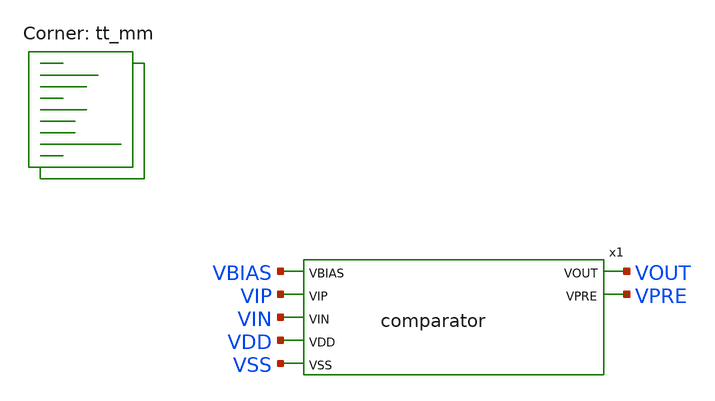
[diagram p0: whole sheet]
** sch_path: xsch/tb_comparator.sch
**.subckt tb_comparator
x1 VBIAS VOUT VIP VPRE VIN VDD VSS comparator
**** begin user architecture code
.lib $::SKYWATER_MODELS/sky130.lib.spice tt_mm

.option method=gear
.option wnflag=1
.option savecurrents

.param VDDGAUSS = agauss(1.8, 0.05, 1)
.param VDD = 'VDDGAUSS'

*.param VBIASGAUSS = agauss(0.7, 0.05, 1)
*.param VBIAS = 'VBIASGAUSS'

.param TEMPGAUSS = agauss(40, 30, 1)
.option temp = 'TEMPGAUSS'

.include stimuli_comparator.cir

Vvdd VDD VSS DC 'VDDGAUSS'

.control
  option seed=9
  let run = 0

  dowhile run < 50
    save all
    save @m5[id]
    tran 100n 1100u uic
    remzerovec
    write tb_comp.raw
    set appendwrite
    reset
    let run = run + 1
end
.endc


**** end user architecture code
**.ends

* expanding   symbol:  /foss/designs/xsch/comparator.sym # of pins=7
** sym_path: xsch/comparator.sym
** sch_path: xsch/comparator.sch
.subckt comparator VBIAS VOUT VIP VPRE VIN VDD VSS
*.ipin VIP
*.ipin VIN
*.ipin VDD
*.ipin VSS
*.ipin VBIAS
*.opin VOUT
*.opin VPRE
XM1 net1 VIN net2 VSS sky130_fd_pr__nfet_01v8 L=1 W=10 nf=1 ad='int((1 + 1)/2) * 10 / 1 * 0.29' as='int((1 + 2)/2) * 10 / 1 * 0.29'
+ pd='2*int((1 + 1)/2) * (10 / 1 + 0.29)' ps='2*int((1 + 2)/2) * (10 / 1 + 0.29)' nrd='0.29 / 10 ' nrs='0.29 / 10 '
+ sa=0 sb=0 sd=0 mult=1 m=1
XM2 VPRE VIP net2 VSS sky130_fd_pr__nfet_01v8 L=1 W=10 nf=1 ad='int((1 + 1)/2) * 10 / 1 * 0.29' as='int((1 + 2)/2) * 10 / 1 * 0.29'
+ pd='2*int((1 + 1)/2) * (10 / 1 + 0.29)' ps='2*int((1 + 2)/2) * (10 / 1 + 0.29)' nrd='0.29 / 10 ' nrs='0.29 / 10 '
+ sa=0 sb=0 sd=0 mult=1 m=1
XM4 VPRE net1 VDD VDD sky130_fd_pr__pfet_01v8 L=1 W=20 nf=1 ad='int((1 + 1)/2) * 20 / 1 * 0.29' as='int((1 + 2)/2) * 20 / 1 * 0.29'
+ pd='2*int((1 + 1)/2) * (20 / 1 + 0.29)' ps='2*int((1 + 2)/2) * (20 / 1 + 0.29)' nrd='0.29 / 20 ' nrs='0.29 / 20 '
+ sa=0 sb=0 sd=0 mult=1 m=1
XM3 net1 net1 VDD VDD sky130_fd_pr__pfet_01v8 L=1 W=20 nf=1 ad='int((1 + 1)/2) * 20 / 1 * 0.29' as='int((1 + 2)/2) * 20 / 1 * 0.29'
+ pd='2*int((1 + 1)/2) * (20 / 1 + 0.29)' ps='2*int((1 + 2)/2) * (20 / 1 + 0.29)' nrd='0.29 / 20 ' nrs='0.29 / 20 '
+ sa=0 sb=0 sd=0 mult=1 m=1
XM5 net2 VBIAS VSS VSS sky130_fd_pr__nfet_01v8 L=1 W=10 nf=1 ad='int((1 + 1)/2) * 10 / 1 * 0.29' as='int((1 + 2)/2) * 10 / 1 * 0.29'
+ pd='2*int((1 + 1)/2) * (10 / 1 + 0.29)' ps='2*int((1 + 2)/2) * (10 / 1 + 0.29)' nrd='0.29 / 10 ' nrs='0.29 / 10 '
+ sa=0 sb=0 sd=0 mult=1 m=1
XM6 VOUT VPRE VDD VDD sky130_fd_pr__pfet_01v8 L=1 W=7 nf=1 ad='int((1 + 1)/2) * 7 / 1 * 0.29' as='int((1 + 2)/2) * 7 / 1 * 0.29'
+ pd='2*int((1 + 1)/2) * (7 / 1 + 0.29)' ps='2*int((1 + 2)/2) * (7 / 1 + 0.29)' nrd='0.29 / 7 ' nrs='0.29 / 7 '
+ sa=0 sb=0 sd=0 mult=1 m=1
XM7 VOUT VPRE VSS VSS sky130_fd_pr__nfet_01v8 L=1 W=3.5 nf=1 ad='int((1 + 1)/2) * 3.5 / 1 * 0.29' as='int((1 + 2)/2) * 3.5 / 1 * 0.29'
+ pd='2*int((1 + 1)/2) * (3.5 / 1 + 0.29)' ps='2*int((1 + 2)/2) * (3.5 / 1 + 0.29)' nrd='0.29 / 3.5 ' nrs='0.29 / 3.5 '
+ sa=0 sb=0 sd=0 mult=1 m=1
XM8 VBIAS VBIAS VSS VSS sky130_fd_pr__nfet_01v8 L=1 W=10 nf=1 ad='int((1 + 1)/2) * 10 / 1 * 0.29' as='int((1 + 2)/2) * 10 / 1 * 0.29'
+ pd='2*int((1 + 1)/2) * (10 / 1 + 0.29)' ps='2*int((1 + 2)/2) * (10 / 1 + 0.29)' nrd='0.29 / 10 ' nrs='0.29 / 10 '
+ sa=0 sb=0 sd=0 mult=1 m=1
R1 VDD VBIAS 1k m=1
.ends

.end
